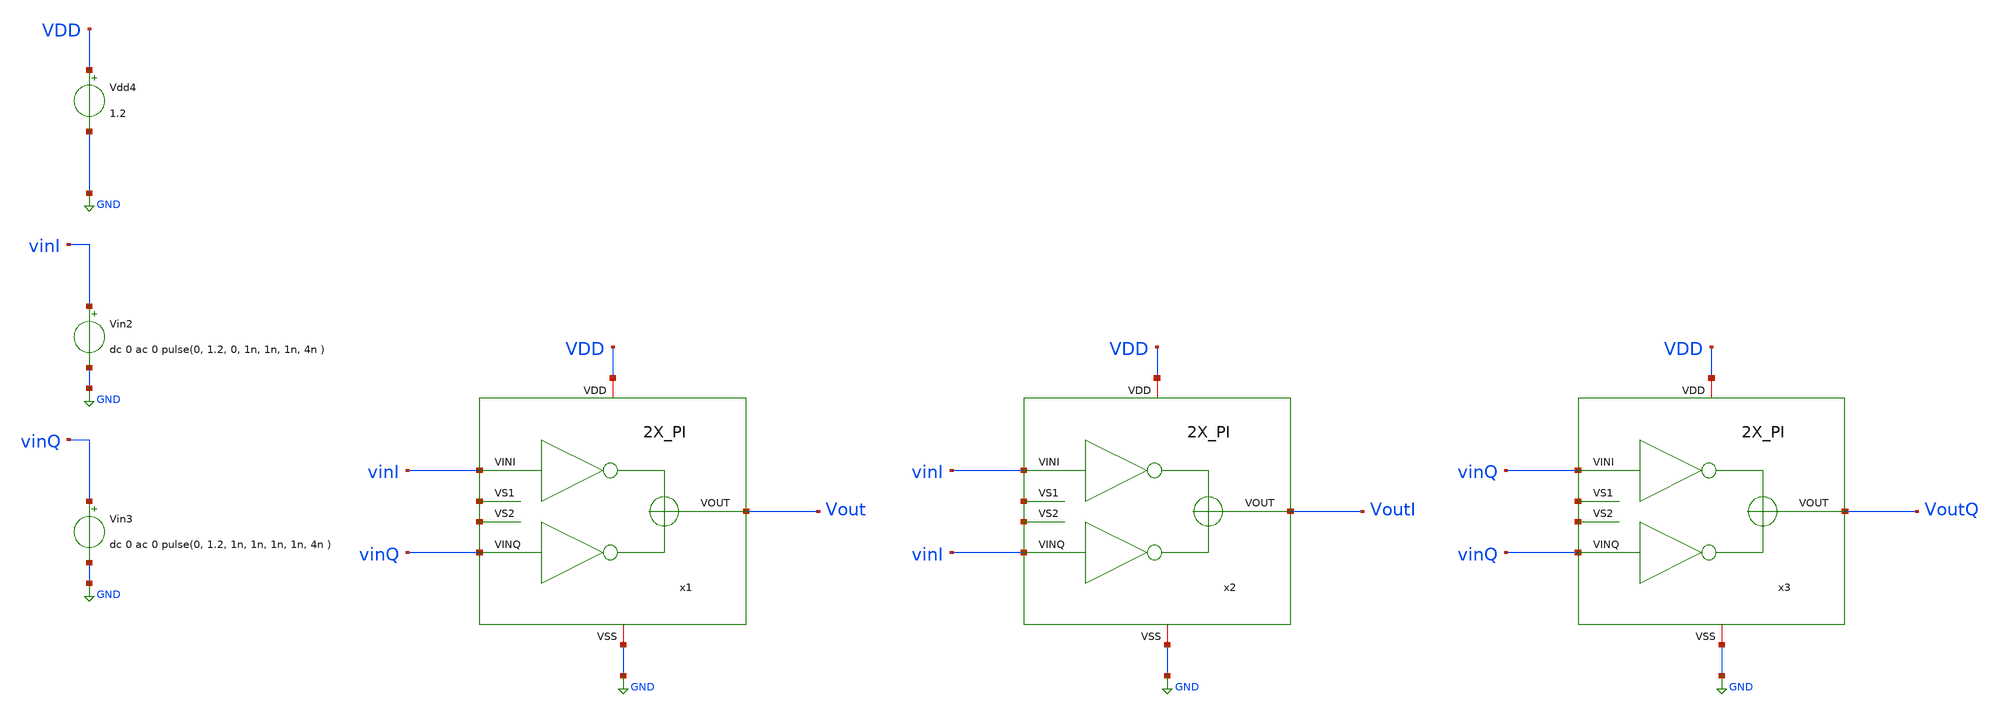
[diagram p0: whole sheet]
** sch_path: others/tb_2X_PI_2.sch
**.subckt tb_2X_PI_2
Vdd4 VDD GND 1.2
Vin2 vinI GND dc 0 ac 0 pulse(0, 1.2, 0, 1n, 1n, 1n, 4n )
Vin3 vinQ GND dc 0 ac 0 pulse(0, 1.2, 1n, 1n, 1n, 1n, 4n )
x1 VDD vinI Vout vinQ GND net1 net2 2X_PI
x2 VDD vinI VoutI vinI GND net3 net4 2X_PI
x3 VDD vinQ VoutQ vinQ GND net5 net6 2X_PI
**** begin user architecture code


.param temp=27
.control
save all
tran 5p 10n
meas tran tdelay TRIG v(in) VAl=0.9 FALl=1 TARG v(out) VAl=0.9 RISE=1
write tran_logic_not.raw
.endc



.lib cornerMOSlv.lib mos_tt

**** end user architecture code
**.ends
.GLOBAL GND
.end
